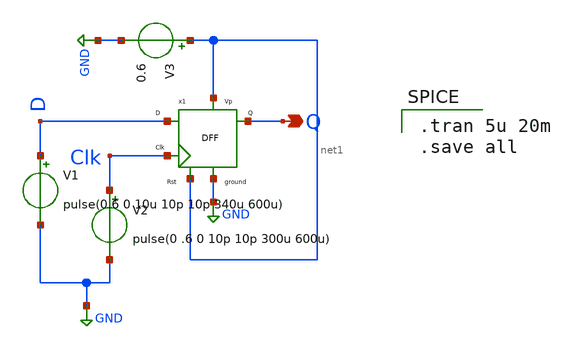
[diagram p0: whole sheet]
** sch_path: untitled-1.sch
**.subckt untitled-1 Q
*.opin Q
x1 D Clk net1 GND net1 Q DFF
V1 D GND pulse(0.6 0 10u 10p 10p 340u 600u)
V2 Clk GND pulse(0 .6 0 10p 10p 300u 600u)
V3 net1 GND 0.6
**** begin user architecture code

** opencircuitdesign pdks install
.lib $::SKYWATER_MODELS/sky130.lib.spice tt



.tran 5u 20m
.save all

**** end user architecture code
**.ends

* expanding   symbol:  component/FlipFlops/DFF.sym # of pins=6
** sym_path: component/FlipFlops/DFF.sym
** sch_path: component/FlipFlops/DFF.sch
.subckt DFF D Clk RST VN VP Q
*.opin Q
*.iopin VN
*.iopin VP
*.ipin Clk
*.ipin D
*.ipin RST
x1 net2 net5 net4 VP VN NAND
x7 net4 Clk RST VP VN net2 NAND3
x3 Q net1 RST VP VN net3 NAND3
x4 net2 Clk net5 VP VN net1 NAND3
x5 net1 D RST VP VN net5 NAND3
x6 net3 net2 Q VP VN NAND
.ends


* expanding   symbol:  component/NAND2/NAND.sym # of pins=5
** sym_path: component/NAND2/NAND.sym
** sch_path: component/NAND2/NAND.sch
.subckt NAND B A Y VP VN
*.iopin VP
*.ipin A
*.ipin B
*.opin Y
*.iopin VN
XM1 Y A VP VP sky130_fd_pr__pfet_01v8 L=0.15 W=1.26 nf=1 ad='int((nf+1)/2) * W/nf * 0.29' as='int((nf+2)/2) * W/nf * 0.29'
+ pd='2*int((nf+1)/2) * (W/nf + 0.29)' ps='2*int((nf+2)/2) * (W/nf + 0.29)' nrd='0.29 / W' nrs='0.29 / W'
+ sa=0 sb=0 sd=0 mult=1 m=1
XM2 Y B VP VP sky130_fd_pr__pfet_01v8 L=0.15 W=1.26 nf=1 ad='int((nf+1)/2) * W/nf * 0.29' as='int((nf+2)/2) * W/nf * 0.29'
+ pd='2*int((nf+1)/2) * (W/nf + 0.29)' ps='2*int((nf+2)/2) * (W/nf + 0.29)' nrd='0.29 / W' nrs='0.29 / W'
+ sa=0 sb=0 sd=0 mult=1 m=1
XM3 Y A net1 net1 sky130_fd_pr__nfet_01v8 L=0.15 W=0.84 nf=1 ad='int((nf+1)/2) * W/nf * 0.29' as='int((nf+2)/2) * W/nf * 0.29'
+ pd='2*int((nf+1)/2) * (W/nf + 0.29)' ps='2*int((nf+2)/2) * (W/nf + 0.29)' nrd='0.29 / W' nrs='0.29 / W'
+ sa=0 sb=0 sd=0 mult=1 m=1
XM4 net1 B VN VN sky130_fd_pr__nfet_01v8 L=0.15 W=0.84 nf=1 ad='int((nf+1)/2) * W/nf * 0.29' as='int((nf+2)/2) * W/nf * 0.29'
+ pd='2*int((nf+1)/2) * (W/nf + 0.29)' ps='2*int((nf+2)/2) * (W/nf + 0.29)' nrd='0.29 / W' nrs='0.29 / W'
+ sa=0 sb=0 sd=0 mult=1 m=1
.ends


* expanding   symbol:  component/NAND3/NAND3.sym # of pins=6
** sym_path: component/NAND3/NAND3.sym
** sch_path: component/NAND3/NAND3.sch
.subckt NAND3 A B C VP VN Y
*.iopin VP
*.iopin VN
*.ipin A
*.ipin B
*.ipin C
*.opin Y
XM1 Y A net1 VN sky130_fd_pr__nfet_01v8 L=0.15 W=1.26 nf=1 ad='int((nf+1)/2) * W/nf * 0.29' as='int((nf+2)/2) * W/nf * 0.29'
+ pd='2*int((nf+1)/2) * (W/nf + 0.29)' ps='2*int((nf+2)/2) * (W/nf + 0.29)' nrd='0.29 / W' nrs='0.29 / W'
+ sa=0 sb=0 sd=0 mult=1 m=1
XM2 net1 B net2 VN sky130_fd_pr__nfet_01v8 L=0.15 W=1.26 nf=1 ad='int((nf+1)/2) * W/nf * 0.29' as='int((nf+2)/2) * W/nf * 0.29'
+ pd='2*int((nf+1)/2) * (W/nf + 0.29)' ps='2*int((nf+2)/2) * (W/nf + 0.29)' nrd='0.29 / W' nrs='0.29 / W'
+ sa=0 sb=0 sd=0 mult=1 m=1
XM3 net2 C VN VN sky130_fd_pr__nfet_01v8 L=0.15 W=1.26 nf=1 ad='int((nf+1)/2) * W/nf * 0.29' as='int((nf+2)/2) * W/nf * 0.29'
+ pd='2*int((nf+1)/2) * (W/nf + 0.29)' ps='2*int((nf+2)/2) * (W/nf + 0.29)' nrd='0.29 / W' nrs='0.29 / W'
+ sa=0 sb=0 sd=0 mult=1 m=1
XM4 Y A VP VP sky130_fd_pr__pfet_01v8 L=0.15 W=1.26 nf=1 ad='int((nf+1)/2) * W/nf * 0.29' as='int((nf+2)/2) * W/nf * 0.29'
+ pd='2*int((nf+1)/2) * (W/nf + 0.29)' ps='2*int((nf+2)/2) * (W/nf + 0.29)' nrd='0.29 / W' nrs='0.29 / W'
+ sa=0 sb=0 sd=0 mult=1 m=1
XM5 Y B VP VP sky130_fd_pr__pfet_01v8 L=0.15 W=1.26 nf=1 ad='int((nf+1)/2) * W/nf * 0.29' as='int((nf+2)/2) * W/nf * 0.29'
+ pd='2*int((nf+1)/2) * (W/nf + 0.29)' ps='2*int((nf+2)/2) * (W/nf + 0.29)' nrd='0.29 / W' nrs='0.29 / W'
+ sa=0 sb=0 sd=0 mult=1 m=1
XM6 Y C VP VP sky130_fd_pr__pfet_01v8 L=0.15 W=1.26 nf=1 ad='int((nf+1)/2) * W/nf * 0.29' as='int((nf+2)/2) * W/nf * 0.29'
+ pd='2*int((nf+1)/2) * (W/nf + 0.29)' ps='2*int((nf+2)/2) * (W/nf + 0.29)' nrd='0.29 / W' nrs='0.29 / W'
+ sa=0 sb=0 sd=0 mult=1 m=1
.ends

.GLOBAL GND
.end
